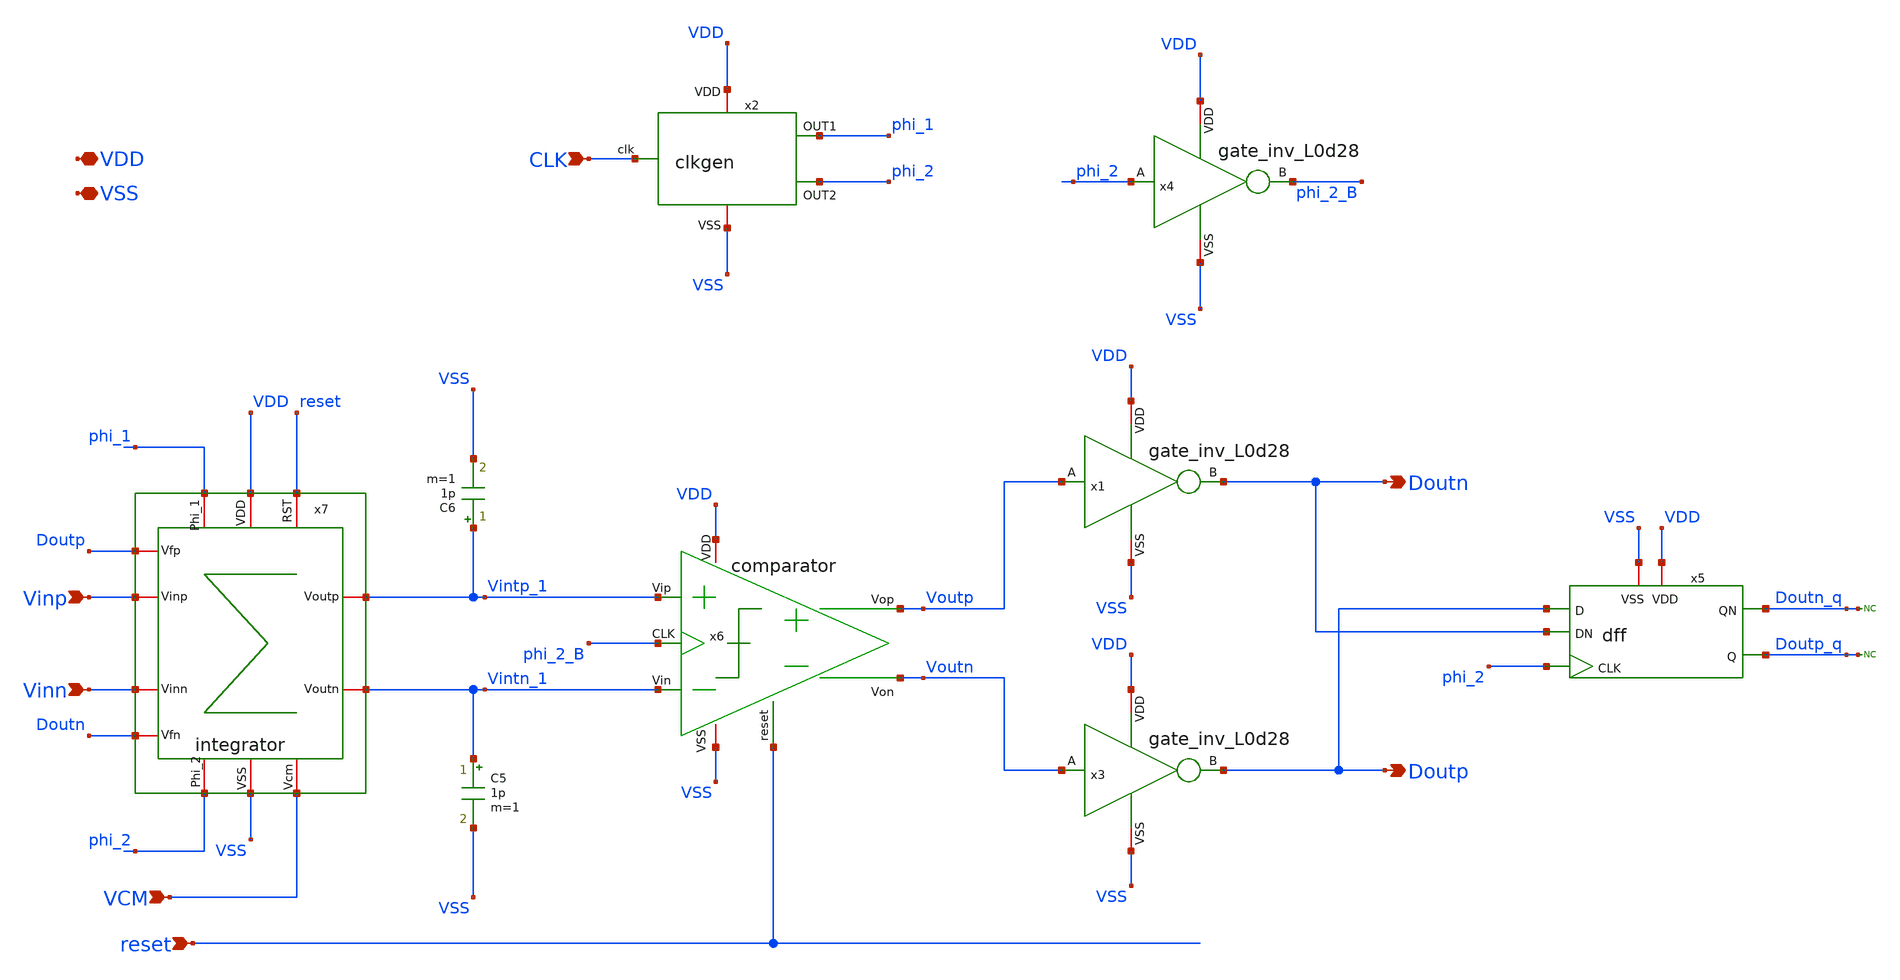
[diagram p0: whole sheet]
** sch_path: designs/DS_modulator/DSM_TOP_1or/xschem/DSM_1st_TOP.sch
**.subckt DSM_1st_TOP reset VDD VSS Doutp Doutn CLK Vinp Vinn VCM
*.ipin reset
*.iopin VDD
*.iopin VSS
*.opin Doutp
*.opin Doutn
*.ipin CLK
*.ipin Vinp
*.ipin Vinn
*.ipin VCM
C5 Vintn_1 VSS 1p m=1
C6 Vintp_1 VSS 1p m=1
* noconn Doutp_q
* noconn Doutn_q
x2 VDD CLK phi_1 phi_2 VSS clkgen
x5 VDD Doutn_q Doutp_q phi_2 VSS Doutp Doutn dff
x6 VDD phi_2_B Voutp reset Voutn Vintp_1 Vintn_1 VSS comparator
x7 reset Vinp VDD phi_1 Vintp_1 VCM Vintn_1 phi_2 VSS Vinn Doutp Doutn integrator
x1 VDD Doutn Voutp VSS gate_inv_L0d28
x3 VDD Doutp Voutn VSS gate_inv_L0d28
x4 VDD phi_2_B phi_2 VSS gate_inv_L0d28
**.ends
.end
